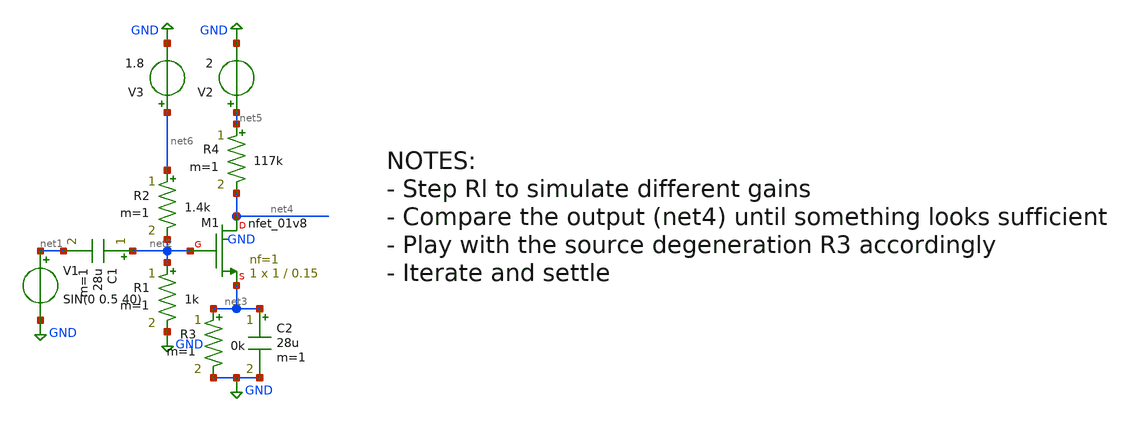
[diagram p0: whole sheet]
** sch_path: xschem/lownoiseamplifier/cs-abstract.sch
**.subckt cs-abstract
XM1 net4 net2 net3 GND sky130_fd_pr__nfet_01v8 L=0.15 W=1 nf=1 ad='int((nf+1)/2) * W/nf * 0.29' as='int((nf+2)/2) * W/nf * 0.29'
+ pd='2*int((nf+1)/2) * (W/nf + 0.29)' ps='2*int((nf+2)/2) * (W/nf + 0.29)' nrd='0.29 / W' nrs='0.29 / W'
+ sa=0 sb=0 sd=0 mult=1 m=1
V1 net1 GND SIN(0 0.5 40)
C1 net2 net1 28u m=1
R1 net2 GND 1k m=1
R2 net6 net2 1.4k m=1
R3 net3 GND 0k m=1
C2 net3 GND 28u m=1
R4 net5 net4 117k m=1
V2 net5 GND 2
V3 net6 GND 1.8
**** begin user architecture code
 ** manual skywater pdks install (with patches applied)
* .lib $::SKYWATER_MODELS/models/sky130.lib.spice tt

** opencircuitdesign pdks install
.lib $::SKYWATER_MODELS/sky130.lib.spice tt

.param mc_mm_switch=0
.param mc_pr_switch=0



.tran 0.001s 0.1s
.control
  run
  plot v(net4) v(net2)
  plot -i(v2)
.endc
.save all


**** end user architecture code
**.ends
.GLOBAL GND
.end
